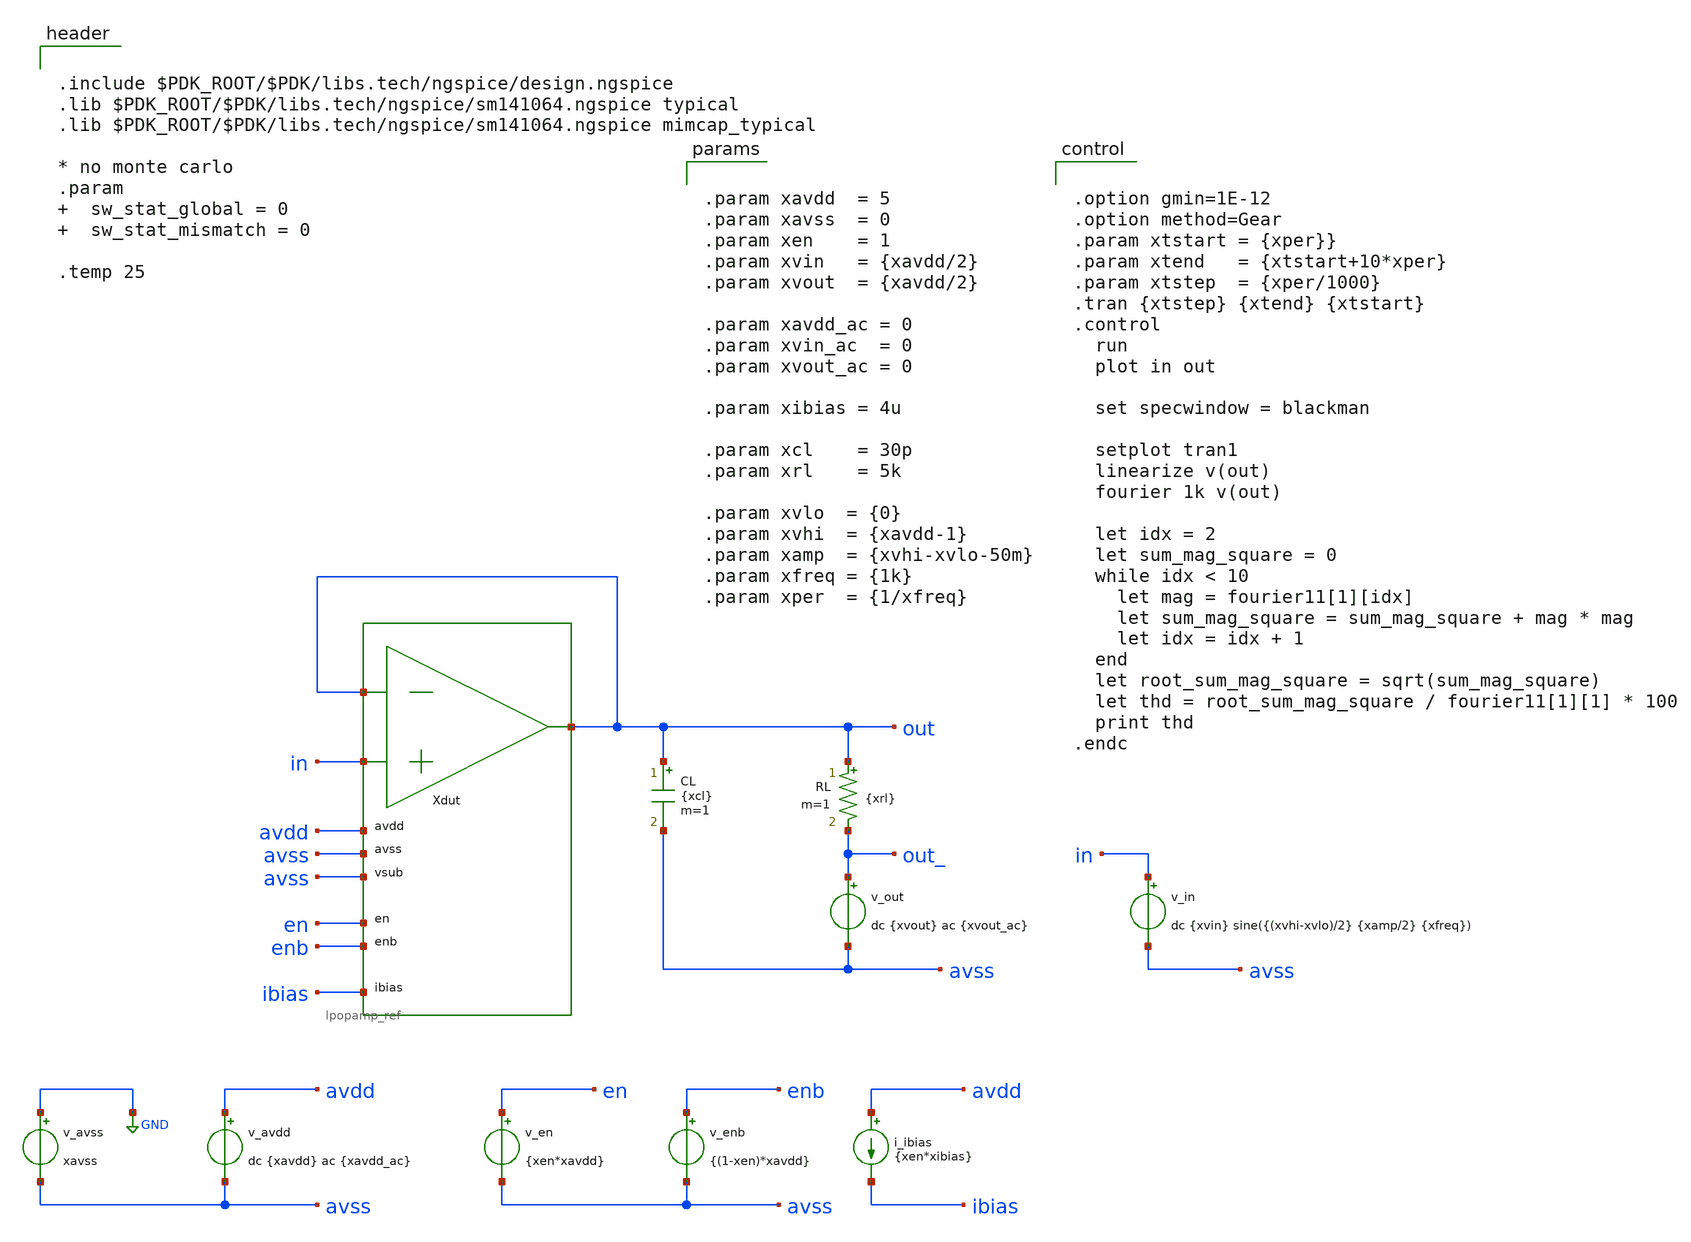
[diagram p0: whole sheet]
** sch_path: xschem/tb_lpopamp_buf_tran_sine.sch
**.subckt tb_lpopamp_buf_tran_sine
Xdut out in out avdd avss avss en enb ibias lpopamp_ref
v_avss GND avss xavss
v_avdd avdd avss dc {xavdd} ac {xavdd_ac}
v_in in avss dc {xvin} sine({(xvhi-xvlo)/2} {xamp/2} {xfreq})
v_en en avss {xen*xavdd}
v_enb enb avss {(1-xen)*xavdd}
i_ibias avdd ibias {xen*xibias}
CL out avss {xcl} m=1
v_out out_ avss dc {xvout} ac {xvout_ac}
RL out out_ {xrl} m=1
**** begin user architecture code


.include $PDK_ROOT/$PDK/libs.tech/ngspice/design.ngspice
.lib $PDK_ROOT/$PDK/libs.tech/ngspice/sm141064.ngspice typical
.lib $PDK_ROOT/$PDK/libs.tech/ngspice/sm141064.ngspice mimcap_typical

* no monte carlo
.param   sw_stat_global = 0   sw_stat_mismatch = 0

.temp 25




.option gmin=1E-12
.option method=Gear
.param xtstart = {xper}}
.param xtend   = {xtstart+10*xper}
.param xtstep  = {xper/1000}
.tran {xtstep} {xtend} {xtstart}
.control
  run
  plot in out

  set specwindow = blackman

  setplot tran1
  linearize v(out)
  fourier 1k v(out)

  let idx = 2
  let sum_mag_square = 0
  while idx < 10
    let mag = fourier11[1][idx]
    let sum_mag_square = sum_mag_square + mag * mag
    let idx = idx + 1
  end
  let root_sum_mag_square = sqrt(sum_mag_square)
  let thd = root_sum_mag_square / fourier11[1][1] * 100
  print thd
.endc




.param xavdd  = 5
.param xavss  = 0
.param xen    = 1
.param xvin   = {xavdd/2}
.param xvout  = {xavdd/2}

.param xavdd_ac = 0
.param xvin_ac  = 0
.param xvout_ac = 0

.param xibias = 4u

.param xcl    = 30p
.param xrl    = 5k

.param xvlo  = {0}
.param xvhi  = {xavdd-1}
.param xamp  = {xvhi-xvlo-50m}
.param xfreq = {1k}
.param xper  = {1/xfreq}


**** end user architecture code
**.ends
.GLOBAL GND
.end
